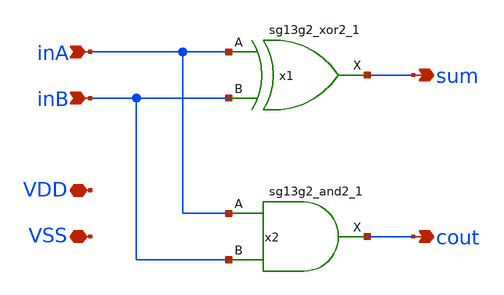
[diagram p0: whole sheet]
** sch_path: 30_MHz_Fractional_N_PLL/design_data/xschem/HALF_ADD.sch
**.subckt HALF_ADD inA inB sum cout VSS VDD
*.ipin inA
*.ipin inB
*.opin sum
*.opin cout
*.iopin VSS
*.iopin VDD
x1 sum inA inB VDD VSS sg13g2_xor2_1
x2 cout inA inB VDD VSS sg13g2_and2_1
**.ends

* expanding   symbol:  sg13g2_stdcells/sg13g2_xor2_1.sym # of pins=3
** sym_path: sg13g2_stdcells/sg13g2_xor2_1.sym
** sch_path: sg13g2_stdcells/sg13g2_xor2_1.sch
.subckt sg13g2_xor2_1 X A B VDD VSS
*.opin X
*.ipin B
*.ipin A
*.iopin VDD
*.iopin VSS
XM1 net1 A VSS VSS sg13_lv_nmos w=550.00n l=130.00n ng=1 m=1 mm_ok=1
XM2 net1 B VSS VSS sg13_lv_nmos w=550.00n l=130.00n ng=1 m=1 mm_ok=1
XM3 X net1 VSS VSS sg13_lv_nmos w=740.00n l=130.00n ng=1 m=1 mm_ok=1
XM4 X B net3 VSS sg13_lv_nmos w=740.00n l=130.00n ng=1 m=1 mm_ok=1
XM5 net3 A VSS VSS sg13_lv_nmos w=740.00n l=130.00n ng=1 m=1 mm_ok=1
XM6 net4 A VDD VDD sg13_lv_pmos w=1.000u l=130.00n ng=1 m=1 mm_ok=1
XM7 net1 B net4 VDD sg13_lv_pmos w=1.000u l=130.00n ng=1 m=1 mm_ok=1
XM8 net2 A VDD VDD sg13_lv_pmos w=1.12u l=130.00n ng=1 m=1 mm_ok=1
XM9 X net1 net2 VDD sg13_lv_pmos w=1.12u l=130.00n ng=1 m=1 mm_ok=1
XM10 net2 B VDD VDD sg13_lv_pmos w=1.12u l=130.00n ng=1 m=1 mm_ok=1
.ends


* expanding   symbol:  sg13g2_stdcells/sg13g2_and2_1.sym # of pins=3
** sym_path: sg13g2_stdcells/sg13g2_and2_1.sym
** sch_path: sg13g2_stdcells/sg13g2_and2_1.sch
.subckt sg13g2_and2_1 X A B VDD VSS
*.ipin A
*.ipin B
*.opin X
*.iopin VDD
*.iopin VSS
XM1 net1 A net2 VSS sg13_lv_nmos w=640.00n l=130.00n ng=1 m=1 mm_ok=1
XM2 net2 B VSS VSS sg13_lv_nmos w=640.00n l=130.00n ng=1 m=1 mm_ok=1
XM3 X net1 VSS VSS sg13_lv_nmos w=740.00n l=130.00n ng=1 m=1 mm_ok=1
XM4 net1 B VDD VDD sg13_lv_pmos w=840.00n l=130.00n ng=1 m=1 mm_ok=1
XM5 net1 A VDD VDD sg13_lv_pmos w=840.00n l=130.00n ng=1 m=1 mm_ok=1
XM6 X net1 VDD VDD sg13_lv_pmos w=1.12u l=130.00n ng=1 m=1 mm_ok=1
.ends

.end
